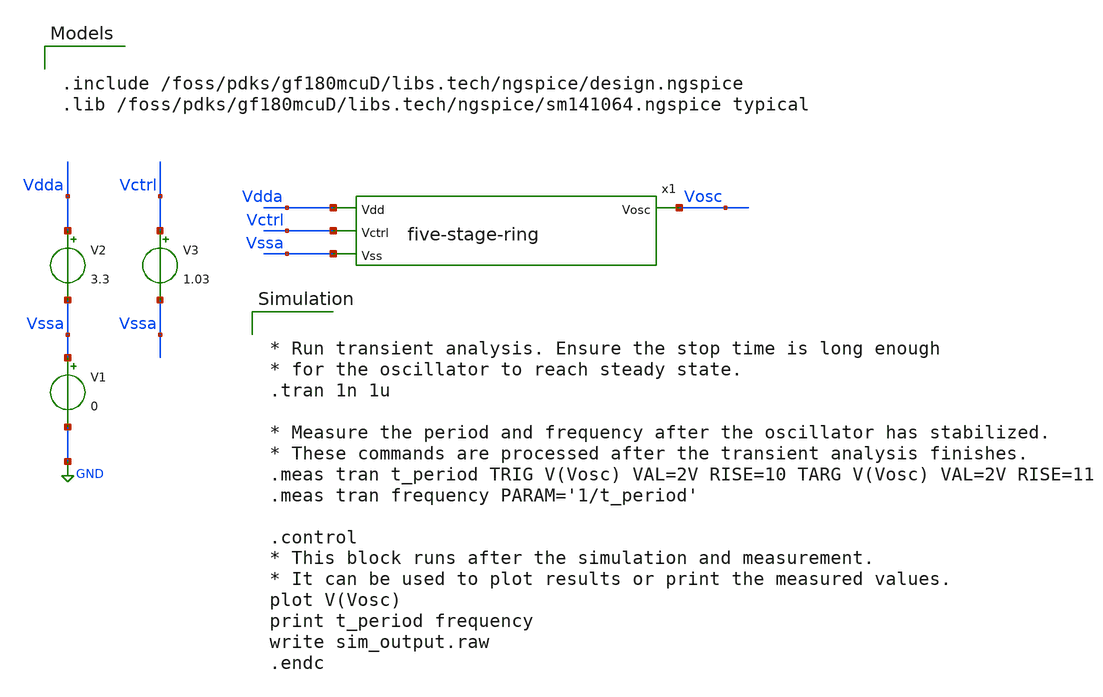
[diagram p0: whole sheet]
** sch_path: Project/1-on-chip/schematic/VCO/ring-vco/tb-five-stage-ring.sch
**.subckt tb-five-stage-ring
V1 Vssa GND 0
V2 Vdda Vssa 3.3
V3 Vctrl Vssa 1.03
x1 Vdda Vosc Vctrl Vssa five-stage-ring
**** begin user architecture code


* Run transient analysis. Ensure the stop time is long enough
* for the oscillator to reach steady state.
.tran 1n 1u

* Measure the period and frequency after the oscillator has stabilized.
* These commands are processed after the transient analysis finishes.
.meas tran t_period TRIG V(Vosc) VAL=2V RISE=10 TARG V(Vosc) VAL=2V RISE=11
.meas tran frequency PARAM='1/t_period'

.control
* This block runs after the simulation and measurement.
* It can be used to plot results or print the measured values.
plot V(Vosc)
print t_period frequency
write sim_output.raw
.endc



.include /foss/pdks/gf180mcuD/libs.tech/ngspice/design.ngspice
.lib /foss/pdks/gf180mcuD/libs.tech/ngspice/sm141064.ngspice typical

**** end user architecture code
**.ends

* expanding   symbol:  gf180mcuD/ring-vco/five-stage-ring.sym # of pins=4
** sym_path: Project/1-on-chip/schematic/VCO/ring-vco/five-stage-ring.sym
** sch_path: Project/1-on-chip/schematic/VCO/ring-vco/five-stage-ring.sch
.subckt five-stage-ring Vdd Vosc Vctrl Vss
*.ipin Vdd
*.ipin Vctrl
*.ipin Vss
*.opin Vosc
XM1 net1 Vosc net5 Vdd pfet_03v3 L=1u W=0.3u nf=4 ad='int((nf+1)/2) * W/nf * 0.18u' as='int((nf+2)/2) * W/nf * 0.18u'
+ pd='2*int((nf+1)/2) * (W/nf + 0.18u)' ps='2*int((nf+2)/2) * (W/nf + 0.18u)' nrd='0.18u / W' nrs='0.18u / W'
+ sa=0 sb=0 sd=0 m=1
XM2 net2 net1 net6 Vdd pfet_03v3 L=1u W=0.3u nf=4 ad='int((nf+1)/2) * W/nf * 0.18u' as='int((nf+2)/2) * W/nf * 0.18u'
+ pd='2*int((nf+1)/2) * (W/nf + 0.18u)' ps='2*int((nf+2)/2) * (W/nf + 0.18u)' nrd='0.18u / W' nrs='0.18u / W'
+ sa=0 sb=0 sd=0 m=1
XM3 net3 net2 net9 Vdd pfet_03v3 L=1u W=0.3u nf=4 ad='int((nf+1)/2) * W/nf * 0.18u' as='int((nf+2)/2) * W/nf * 0.18u'
+ pd='2*int((nf+1)/2) * (W/nf + 0.18u)' ps='2*int((nf+2)/2) * (W/nf + 0.18u)' nrd='0.18u / W' nrs='0.18u / W'
+ sa=0 sb=0 sd=0 m=1
XM4 net4 net3 net8 Vdd pfet_03v3 L=1u W=0.3u nf=4 ad='int((nf+1)/2) * W/nf * 0.18u' as='int((nf+2)/2) * W/nf * 0.18u'
+ pd='2*int((nf+1)/2) * (W/nf + 0.18u)' ps='2*int((nf+2)/2) * (W/nf + 0.18u)' nrd='0.18u / W' nrs='0.18u / W'
+ sa=0 sb=0 sd=0 m=1
XM5 Vosc net4 net7 Vdd pfet_03v3 L=1u W=0.3u nf=4 ad='int((nf+1)/2) * W/nf * 0.18u' as='int((nf+2)/2) * W/nf * 0.18u'
+ pd='2*int((nf+1)/2) * (W/nf + 0.18u)' ps='2*int((nf+2)/2) * (W/nf + 0.18u)' nrd='0.18u / W' nrs='0.18u / W'
+ sa=0 sb=0 sd=0 m=1
XM6 net1 Vosc net11 Vss nfet_03v3 L=1u W=0.3u nf=1 ad='int((nf+1)/2) * W/nf * 0.18u' as='int((nf+2)/2) * W/nf * 0.18u'
+ pd='2*int((nf+1)/2) * (W/nf + 0.18u)' ps='2*int((nf+2)/2) * (W/nf + 0.18u)' nrd='0.18u / W' nrs='0.18u / W'
+ sa=0 sb=0 sd=0 m=1
XM7 net2 net1 net12 Vss nfet_03v3 L=1u W=0.3u nf=1 ad='int((nf+1)/2) * W/nf * 0.18u' as='int((nf+2)/2) * W/nf * 0.18u'
+ pd='2*int((nf+1)/2) * (W/nf + 0.18u)' ps='2*int((nf+2)/2) * (W/nf + 0.18u)' nrd='0.18u / W' nrs='0.18u / W'
+ sa=0 sb=0 sd=0 m=1
XM8 net3 net2 net13 Vss nfet_03v3 L=1u W=0.3u nf=1 ad='int((nf+1)/2) * W/nf * 0.18u' as='int((nf+2)/2) * W/nf * 0.18u'
+ pd='2*int((nf+1)/2) * (W/nf + 0.18u)' ps='2*int((nf+2)/2) * (W/nf + 0.18u)' nrd='0.18u / W' nrs='0.18u / W'
+ sa=0 sb=0 sd=0 m=1
XM9 net4 net3 net14 Vss nfet_03v3 L=1u W=0.3u nf=1 ad='int((nf+1)/2) * W/nf * 0.18u' as='int((nf+2)/2) * W/nf * 0.18u'
+ pd='2*int((nf+1)/2) * (W/nf + 0.18u)' ps='2*int((nf+2)/2) * (W/nf + 0.18u)' nrd='0.18u / W' nrs='0.18u / W'
+ sa=0 sb=0 sd=0 m=1
XM10 Vosc net4 net15 Vss nfet_03v3 L=1u W=0.3u nf=1 ad='int((nf+1)/2) * W/nf * 0.18u' as='int((nf+2)/2) * W/nf * 0.18u'
+ pd='2*int((nf+1)/2) * (W/nf + 0.18u)' ps='2*int((nf+2)/2) * (W/nf + 0.18u)' nrd='0.18u / W' nrs='0.18u / W'
+ sa=0 sb=0 sd=0 m=1
XM11 net5 net10 Vdd Vdd pfet_03v3 L=1u W=0.3u nf=4 ad='int((nf+1)/2) * W/nf * 0.18u' as='int((nf+2)/2) * W/nf * 0.18u'
+ pd='2*int((nf+1)/2) * (W/nf + 0.18u)' ps='2*int((nf+2)/2) * (W/nf + 0.18u)' nrd='0.18u / W' nrs='0.18u / W'
+ sa=0 sb=0 sd=0 m=1
XM12 net6 net10 Vdd Vdd pfet_03v3 L=1u W=0.3u nf=4 ad='int((nf+1)/2) * W/nf * 0.18u' as='int((nf+2)/2) * W/nf * 0.18u'
+ pd='2*int((nf+1)/2) * (W/nf + 0.18u)' ps='2*int((nf+2)/2) * (W/nf + 0.18u)' nrd='0.18u / W' nrs='0.18u / W'
+ sa=0 sb=0 sd=0 m=1
XM13 net9 net10 Vdd Vdd pfet_03v3 L=1u W=0.3u nf=4 ad='int((nf+1)/2) * W/nf * 0.18u' as='int((nf+2)/2) * W/nf * 0.18u'
+ pd='2*int((nf+1)/2) * (W/nf + 0.18u)' ps='2*int((nf+2)/2) * (W/nf + 0.18u)' nrd='0.18u / W' nrs='0.18u / W'
+ sa=0 sb=0 sd=0 m=1
XM14 net8 net10 Vdd Vdd pfet_03v3 L=1u W=0.3u nf=4 ad='int((nf+1)/2) * W/nf * 0.18u' as='int((nf+2)/2) * W/nf * 0.18u'
+ pd='2*int((nf+1)/2) * (W/nf + 0.18u)' ps='2*int((nf+2)/2) * (W/nf + 0.18u)' nrd='0.18u / W' nrs='0.18u / W'
+ sa=0 sb=0 sd=0 m=1
XM15 net7 net10 Vdd Vdd pfet_03v3 L=1u W=0.3u nf=4 ad='int((nf+1)/2) * W/nf * 0.18u' as='int((nf+2)/2) * W/nf * 0.18u'
+ pd='2*int((nf+1)/2) * (W/nf + 0.18u)' ps='2*int((nf+2)/2) * (W/nf + 0.18u)' nrd='0.18u / W' nrs='0.18u / W'
+ sa=0 sb=0 sd=0 m=1
XM16 net10 net10 Vdd Vdd pfet_03v3 L=1u W=0.3u nf=4 ad='int((nf+1)/2) * W/nf * 0.18u' as='int((nf+2)/2) * W/nf * 0.18u'
+ pd='2*int((nf+1)/2) * (W/nf + 0.18u)' ps='2*int((nf+2)/2) * (W/nf + 0.18u)' nrd='0.18u / W' nrs='0.18u / W'
+ sa=0 sb=0 sd=0 m=1
XM17 net11 Vctrl Vss Vss nfet_03v3 L=1u W=0.3u nf=1 ad='int((nf+1)/2) * W/nf * 0.18u' as='int((nf+2)/2) * W/nf * 0.18u'
+ pd='2*int((nf+1)/2) * (W/nf + 0.18u)' ps='2*int((nf+2)/2) * (W/nf + 0.18u)' nrd='0.18u / W' nrs='0.18u / W'
+ sa=0 sb=0 sd=0 m=1
XM18 net12 Vctrl Vss Vss nfet_03v3 L=1u W=0.3u nf=1 ad='int((nf+1)/2) * W/nf * 0.18u' as='int((nf+2)/2) * W/nf * 0.18u'
+ pd='2*int((nf+1)/2) * (W/nf + 0.18u)' ps='2*int((nf+2)/2) * (W/nf + 0.18u)' nrd='0.18u / W' nrs='0.18u / W'
+ sa=0 sb=0 sd=0 m=1
XM19 net13 Vctrl Vss Vss nfet_03v3 L=1u W=0.3u nf=1 ad='int((nf+1)/2) * W/nf * 0.18u' as='int((nf+2)/2) * W/nf * 0.18u'
+ pd='2*int((nf+1)/2) * (W/nf + 0.18u)' ps='2*int((nf+2)/2) * (W/nf + 0.18u)' nrd='0.18u / W' nrs='0.18u / W'
+ sa=0 sb=0 sd=0 m=1
XM20 net14 Vctrl Vss Vss nfet_03v3 L=1u W=0.3u nf=1 ad='int((nf+1)/2) * W/nf * 0.18u' as='int((nf+2)/2) * W/nf * 0.18u'
+ pd='2*int((nf+1)/2) * (W/nf + 0.18u)' ps='2*int((nf+2)/2) * (W/nf + 0.18u)' nrd='0.18u / W' nrs='0.18u / W'
+ sa=0 sb=0 sd=0 m=1
XM21 net15 Vctrl Vss Vss nfet_03v3 L=1u W=0.3u nf=1 ad='int((nf+1)/2) * W/nf * 0.18u' as='int((nf+2)/2) * W/nf * 0.18u'
+ pd='2*int((nf+1)/2) * (W/nf + 0.18u)' ps='2*int((nf+2)/2) * (W/nf + 0.18u)' nrd='0.18u / W' nrs='0.18u / W'
+ sa=0 sb=0 sd=0 m=1
XM22 net10 Vctrl Vss Vss nfet_03v3 L=1u W=0.3u nf=1 ad='int((nf+1)/2) * W/nf * 0.18u' as='int((nf+2)/2) * W/nf * 0.18u'
+ pd='2*int((nf+1)/2) * (W/nf + 0.18u)' ps='2*int((nf+2)/2) * (W/nf + 0.18u)' nrd='0.18u / W' nrs='0.18u / W'
+ sa=0 sb=0 sd=0 m=1
.ends

.GLOBAL GND
.end
